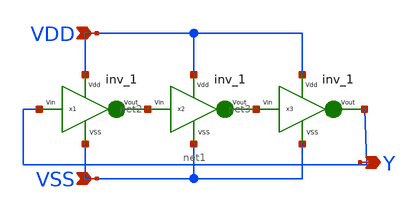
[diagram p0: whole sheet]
** sch_path: xschem files/Ring Oscillator.sch
**.subckt Ring Oscillator VDD Y VSS
*.ipin VDD
*.opin Y
*.ipin VSS
x1 VDD net2 net1 VSS inv_1
x2 VDD net3 net2 VSS inv_1
x3 VDD net1 net3 VSS inv_1
**.ends

* expanding   symbol:  /home/harshit/.xschem/inv_1.sym # of pins=4
** sym_path: xschem files/inv_1.sym
** sch_path: xschem files/inv_1.sch
.subckt inv_1 Vdd Vout Vin VSS
*.ipin Vdd
*.ipin VSS
*.opin Vout
*.ipin Vin
XM1 Vout Vin VSS VSS sky130_fd_pr__nfet_01v8 L=0.15 W=1.05 nf=1 ad='int((nf+1)/2) * W/nf * 0.29' as='int((nf+2)/2) * W/nf * 0.29'
+ pd='2*int((nf+1)/2) * (W/nf + 0.29)' ps='2*int((nf+2)/2) * (W/nf + 0.29)' nrd='0.29 / W' nrs='0.29 / W'
+ sa=0 sb=0 sd=0 mult=1 m=1
XM2 Vout Vin Vdd Vdd sky130_fd_pr__pfet_01v8 L=0.15 W=2.1 nf=1 ad='int((nf+1)/2) * W/nf * 0.29' as='int((nf+2)/2) * W/nf * 0.29'
+ pd='2*int((nf+1)/2) * (W/nf + 0.29)' ps='2*int((nf+2)/2) * (W/nf + 0.29)' nrd='0.29 / W' nrs='0.29 / W'
+ sa=0 sb=0 sd=0 mult=1 m=1
.ends

.end
